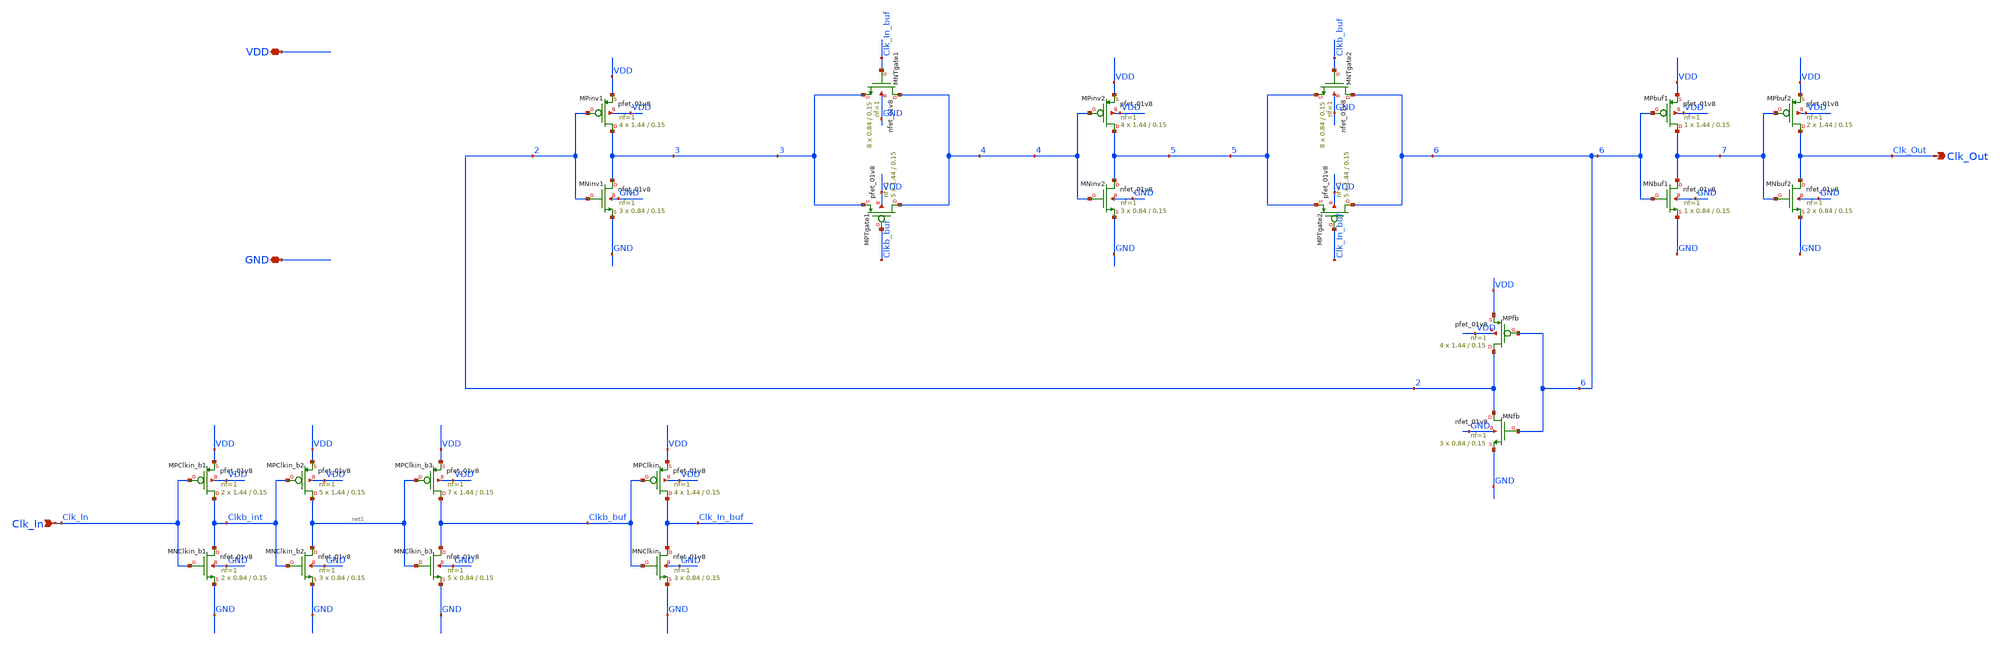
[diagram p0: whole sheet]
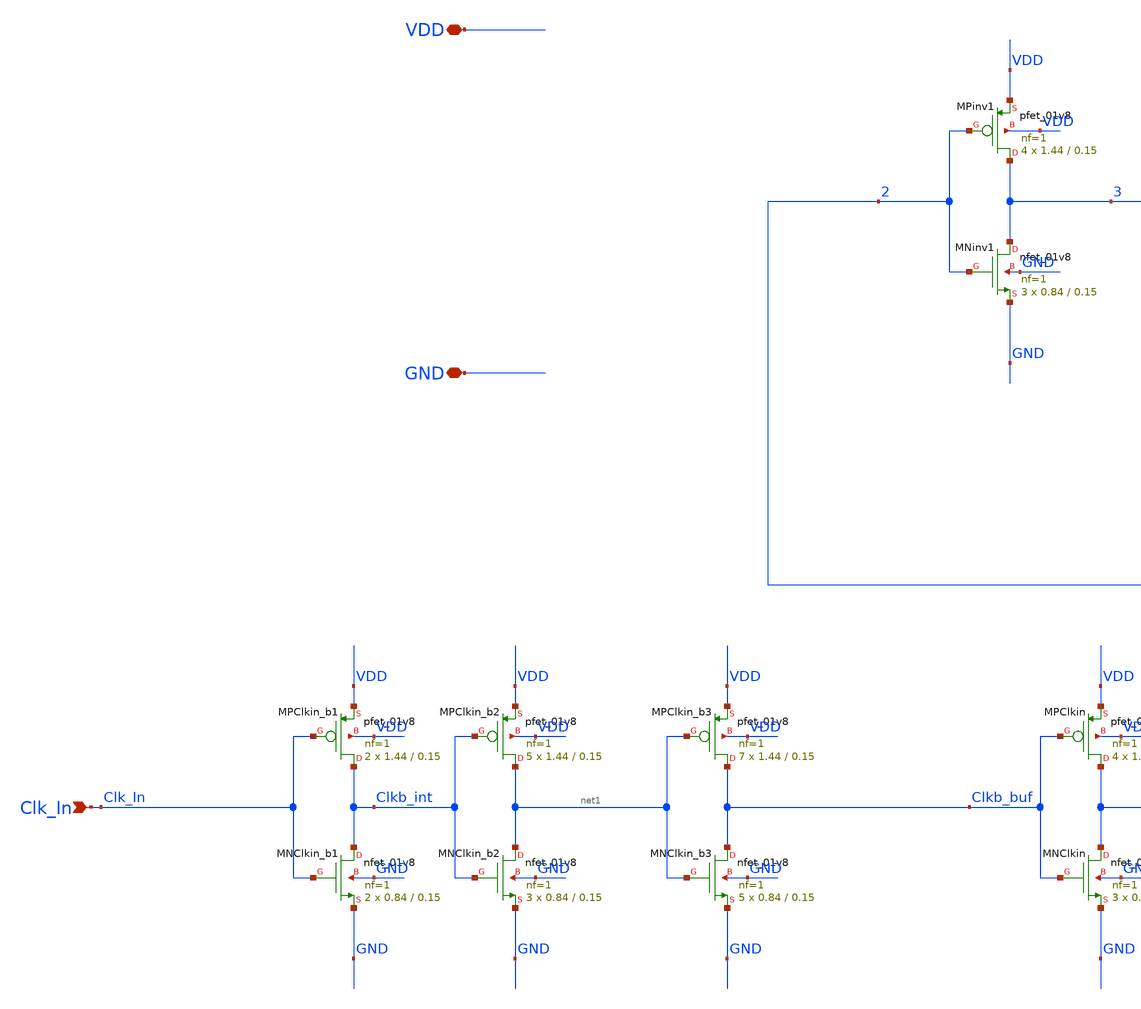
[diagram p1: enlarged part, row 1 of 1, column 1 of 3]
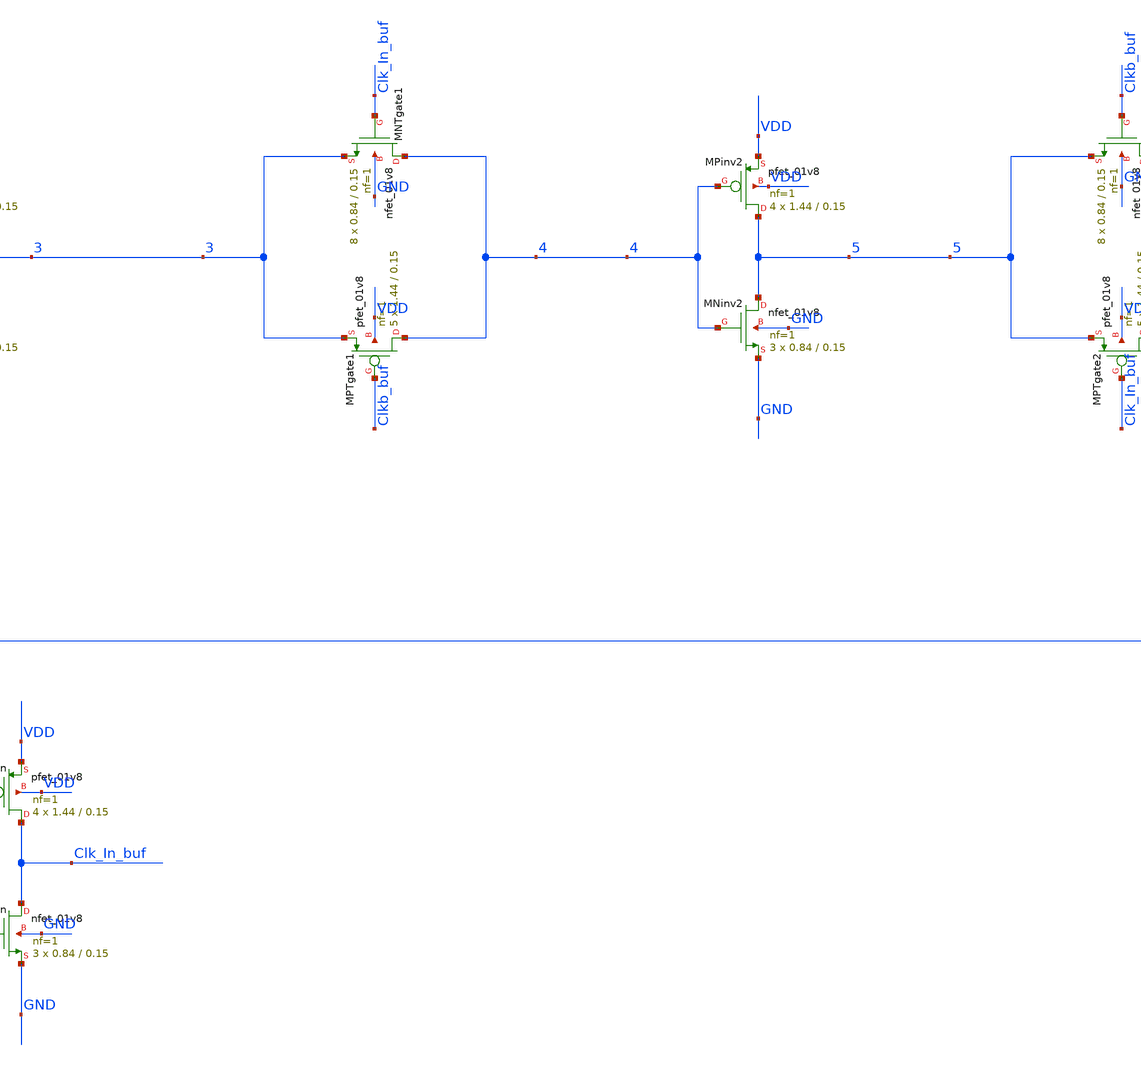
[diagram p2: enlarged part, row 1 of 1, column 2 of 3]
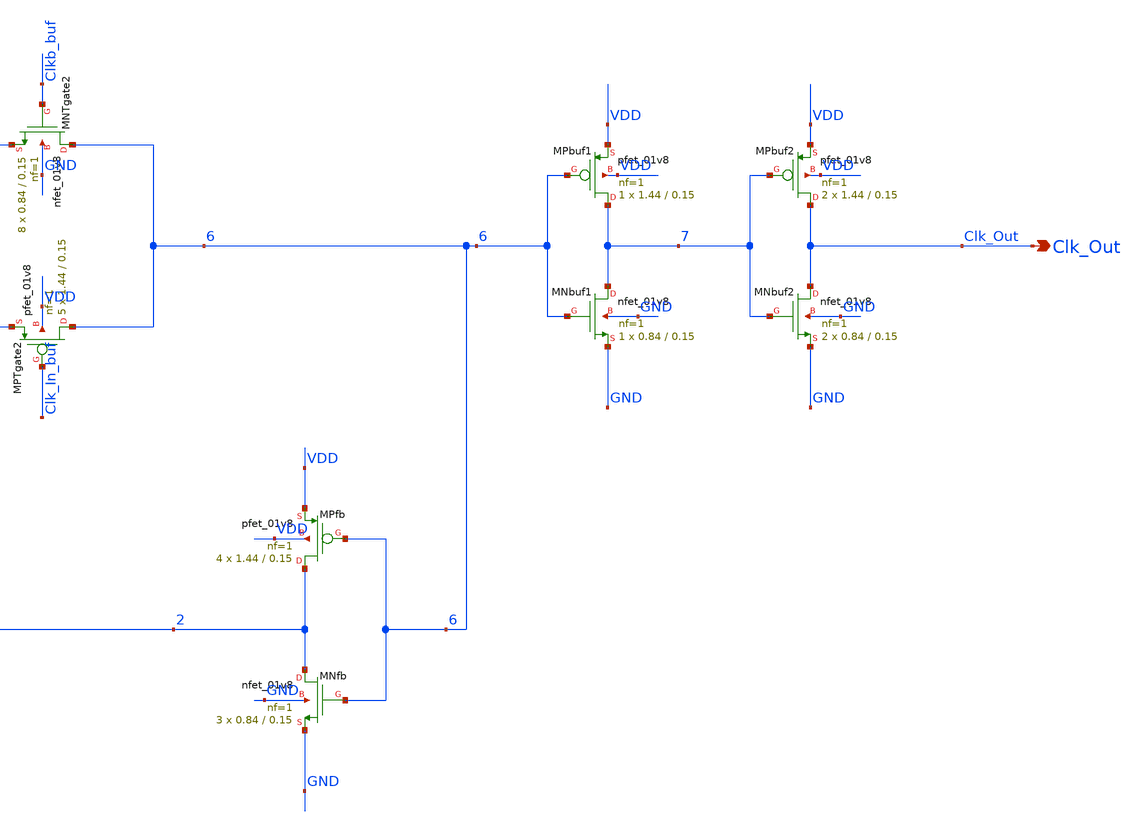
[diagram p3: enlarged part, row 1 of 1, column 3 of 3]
** sch_path: xschem/3-stage_cs-vco_dp9/FD_v5.sch
**.subckt FD_v5 Clk_In VDD GND Clk_Out
*.ipin Clk_In
*.iopin VDD
*.iopin GND
*.opin Clk_Out
XMPbuf1 7 6 VDD VDD sky130_fd_pr__pfet_01v8 L=0.15 W=1.44 nf=1 ad='int((nf+1)/2) * W/nf * 0.29' as='int((nf+2)/2) * W/nf * 0.29'
+ pd='2*int((nf+1)/2) * (W/nf + 0.29)' ps='2*int((nf+2)/2) * (W/nf + 0.29)' nrd='0.29 / W' nrs='0.29 / W'
+ sa=0 sb=0 sd=0 mult=1 m=1
XMNbuf1 7 6 GND GND sky130_fd_pr__nfet_01v8 L=0.15 W=0.84 nf=1 ad='int((nf+1)/2) * W/nf * 0.29' as='int((nf+2)/2) * W/nf * 0.29'
+ pd='2*int((nf+1)/2) * (W/nf + 0.29)' ps='2*int((nf+2)/2) * (W/nf + 0.29)' nrd='0.29 / W' nrs='0.29 / W'
+ sa=0 sb=0 sd=0 mult=1 m=1
XMPClkin Clk_In_buf Clkb_buf VDD VDD sky130_fd_pr__pfet_01v8 L=0.15 W=1.44 nf=1 ad='int((nf+1)/2) * W/nf * 0.29'
+ as='int((nf+2)/2) * W/nf * 0.29' pd='2*int((nf+1)/2) * (W/nf + 0.29)' ps='2*int((nf+2)/2) * (W/nf + 0.29)'
+ nrd='0.29 / W' nrs='0.29 / W' sa=0 sb=0 sd=0 mult=4 m=4
XMNClkin Clk_In_buf Clkb_buf GND GND sky130_fd_pr__nfet_01v8 L=0.15 W=0.84 nf=1 ad='int((nf+1)/2) * W/nf * 0.29'
+ as='int((nf+2)/2) * W/nf * 0.29' pd='2*int((nf+1)/2) * (W/nf + 0.29)' ps='2*int((nf+2)/2) * (W/nf + 0.29)'
+ nrd='0.29 / W' nrs='0.29 / W' sa=0 sb=0 sd=0 mult=3 m=3
XMPinv2 5 4 VDD VDD sky130_fd_pr__pfet_01v8 L=0.15 W=1.44 nf=1 ad='int((nf+1)/2) * W/nf * 0.29' as='int((nf+2)/2) * W/nf * 0.29'
+ pd='2*int((nf+1)/2) * (W/nf + 0.29)' ps='2*int((nf+2)/2) * (W/nf + 0.29)' nrd='0.29 / W' nrs='0.29 / W'
+ sa=0 sb=0 sd=0 mult=4 m=4
XMNinv2 5 4 GND GND sky130_fd_pr__nfet_01v8 L=0.15 W=0.84 nf=1 ad='int((nf+1)/2) * W/nf * 0.29' as='int((nf+2)/2) * W/nf * 0.29'
+ pd='2*int((nf+1)/2) * (W/nf + 0.29)' ps='2*int((nf+2)/2) * (W/nf + 0.29)' nrd='0.29 / W' nrs='0.29 / W'
+ sa=0 sb=0 sd=0 mult=3 m=3
XMPinv1 3 2 VDD VDD sky130_fd_pr__pfet_01v8 L=0.15 W=1.44 nf=1 ad='int((nf+1)/2) * W/nf * 0.29' as='int((nf+2)/2) * W/nf * 0.29'
+ pd='2*int((nf+1)/2) * (W/nf + 0.29)' ps='2*int((nf+2)/2) * (W/nf + 0.29)' nrd='0.29 / W' nrs='0.29 / W'
+ sa=0 sb=0 sd=0 mult=4 m=4
XMNinv1 3 2 GND GND sky130_fd_pr__nfet_01v8 L=0.15 W=0.84 nf=1 ad='int((nf+1)/2) * W/nf * 0.29' as='int((nf+2)/2) * W/nf * 0.29'
+ pd='2*int((nf+1)/2) * (W/nf + 0.29)' ps='2*int((nf+2)/2) * (W/nf + 0.29)' nrd='0.29 / W' nrs='0.29 / W'
+ sa=0 sb=0 sd=0 mult=3 m=3
XMPTgate1 4 Clkb_buf 3 VDD sky130_fd_pr__pfet_01v8 L=0.15 W=1.44 nf=1 ad='int((nf+1)/2) * W/nf * 0.29'
+ as='int((nf+2)/2) * W/nf * 0.29' pd='2*int((nf+1)/2) * (W/nf + 0.29)' ps='2*int((nf+2)/2) * (W/nf + 0.29)'
+ nrd='0.29 / W' nrs='0.29 / W' sa=0 sb=0 sd=0 mult=5 m=5
XMNTgate1 4 Clk_In_buf 3 GND sky130_fd_pr__nfet_01v8 L=0.15 W=0.84 nf=1 ad='int((nf+1)/2) * W/nf * 0.29'
+ as='int((nf+2)/2) * W/nf * 0.29' pd='2*int((nf+1)/2) * (W/nf + 0.29)' ps='2*int((nf+2)/2) * (W/nf + 0.29)'
+ nrd='0.29 / W' nrs='0.29 / W' sa=0 sb=0 sd=0 mult=8 m=8
XMPTgate2 6 Clk_In_buf 5 VDD sky130_fd_pr__pfet_01v8 L=0.15 W=1.44 nf=1 ad='int((nf+1)/2) * W/nf * 0.29'
+ as='int((nf+2)/2) * W/nf * 0.29' pd='2*int((nf+1)/2) * (W/nf + 0.29)' ps='2*int((nf+2)/2) * (W/nf + 0.29)'
+ nrd='0.29 / W' nrs='0.29 / W' sa=0 sb=0 sd=0 mult=5 m=5
XMNTgate2 6 Clkb_buf 5 GND sky130_fd_pr__nfet_01v8 L=0.15 W=0.84 nf=1 ad='int((nf+1)/2) * W/nf * 0.29'
+ as='int((nf+2)/2) * W/nf * 0.29' pd='2*int((nf+1)/2) * (W/nf + 0.29)' ps='2*int((nf+2)/2) * (W/nf + 0.29)'
+ nrd='0.29 / W' nrs='0.29 / W' sa=0 sb=0 sd=0 mult=8 m=8
XMPbuf2 Clk_Out 7 VDD VDD sky130_fd_pr__pfet_01v8 L=0.15 W=1.44 nf=1 ad='int((nf+1)/2) * W/nf * 0.29'
+ as='int((nf+2)/2) * W/nf * 0.29' pd='2*int((nf+1)/2) * (W/nf + 0.29)' ps='2*int((nf+2)/2) * (W/nf + 0.29)'
+ nrd='0.29 / W' nrs='0.29 / W' sa=0 sb=0 sd=0 mult=2 m=2
XMNbuf2 Clk_Out 7 GND GND sky130_fd_pr__nfet_01v8 L=0.15 W=0.84 nf=1 ad='int((nf+1)/2) * W/nf * 0.29'
+ as='int((nf+2)/2) * W/nf * 0.29' pd='2*int((nf+1)/2) * (W/nf + 0.29)' ps='2*int((nf+2)/2) * (W/nf + 0.29)'
+ nrd='0.29 / W' nrs='0.29 / W' sa=0 sb=0 sd=0 mult=2 m=2
XMPfb 2 6 VDD VDD sky130_fd_pr__pfet_01v8 L=0.15 W=1.44 nf=1 ad='int((nf+1)/2) * W/nf * 0.29' as='int((nf+2)/2) * W/nf * 0.29'
+ pd='2*int((nf+1)/2) * (W/nf + 0.29)' ps='2*int((nf+2)/2) * (W/nf + 0.29)' nrd='0.29 / W' nrs='0.29 / W'
+ sa=0 sb=0 sd=0 mult=4 m=4
XMNfb 2 6 GND GND sky130_fd_pr__nfet_01v8 L=0.15 W=0.84 nf=1 ad='int((nf+1)/2) * W/nf * 0.29' as='int((nf+2)/2) * W/nf * 0.29'
+ pd='2*int((nf+1)/2) * (W/nf + 0.29)' ps='2*int((nf+2)/2) * (W/nf + 0.29)' nrd='0.29 / W' nrs='0.29 / W'
+ sa=0 sb=0 sd=0 mult=3 m=3
XMPClkin_b2 net1 Clkb_int VDD VDD sky130_fd_pr__pfet_01v8 L=0.15 W=1.44 nf=1 ad='int((nf+1)/2) * W/nf * 0.29'
+ as='int((nf+2)/2) * W/nf * 0.29' pd='2*int((nf+1)/2) * (W/nf + 0.29)' ps='2*int((nf+2)/2) * (W/nf + 0.29)'
+ nrd='0.29 / W' nrs='0.29 / W' sa=0 sb=0 sd=0 mult=5 m=5
XMNClkin_b2 net1 Clkb_int GND GND sky130_fd_pr__nfet_01v8 L=0.15 W=0.84 nf=1 ad='int((nf+1)/2) * W/nf * 0.29'
+ as='int((nf+2)/2) * W/nf * 0.29' pd='2*int((nf+1)/2) * (W/nf + 0.29)' ps='2*int((nf+2)/2) * (W/nf + 0.29)'
+ nrd='0.29 / W' nrs='0.29 / W' sa=0 sb=0 sd=0 mult=3 m=3
XMPClkin_b1 Clkb_int Clk_In VDD VDD sky130_fd_pr__pfet_01v8 L=0.15 W=1.44 nf=1 ad='int((nf+1)/2) * W/nf * 0.29'
+ as='int((nf+2)/2) * W/nf * 0.29' pd='2*int((nf+1)/2) * (W/nf + 0.29)' ps='2*int((nf+2)/2) * (W/nf + 0.29)'
+ nrd='0.29 / W' nrs='0.29 / W' sa=0 sb=0 sd=0 mult=2 m=2
XMNClkin_b1 Clkb_int Clk_In GND GND sky130_fd_pr__nfet_01v8 L=0.15 W=0.84 nf=1 ad='int((nf+1)/2) * W/nf * 0.29'
+ as='int((nf+2)/2) * W/nf * 0.29' pd='2*int((nf+1)/2) * (W/nf + 0.29)' ps='2*int((nf+2)/2) * (W/nf + 0.29)'
+ nrd='0.29 / W' nrs='0.29 / W' sa=0 sb=0 sd=0 mult=2 m=2
XMPClkin_b3 Clkb_buf net1 VDD VDD sky130_fd_pr__pfet_01v8 L=0.15 W=1.44 nf=1 ad='int((nf+1)/2) * W/nf * 0.29'
+ as='int((nf+2)/2) * W/nf * 0.29' pd='2*int((nf+1)/2) * (W/nf + 0.29)' ps='2*int((nf+2)/2) * (W/nf + 0.29)'
+ nrd='0.29 / W' nrs='0.29 / W' sa=0 sb=0 sd=0 mult=7 m=7
XMNClkin_b3 Clkb_buf net1 GND GND sky130_fd_pr__nfet_01v8 L=0.15 W=0.84 nf=1 ad='int((nf+1)/2) * W/nf * 0.29'
+ as='int((nf+2)/2) * W/nf * 0.29' pd='2*int((nf+1)/2) * (W/nf + 0.29)' ps='2*int((nf+2)/2) * (W/nf + 0.29)'
+ nrd='0.29 / W' nrs='0.29 / W' sa=0 sb=0 sd=0 mult=5 m=5
**.ends
.end
